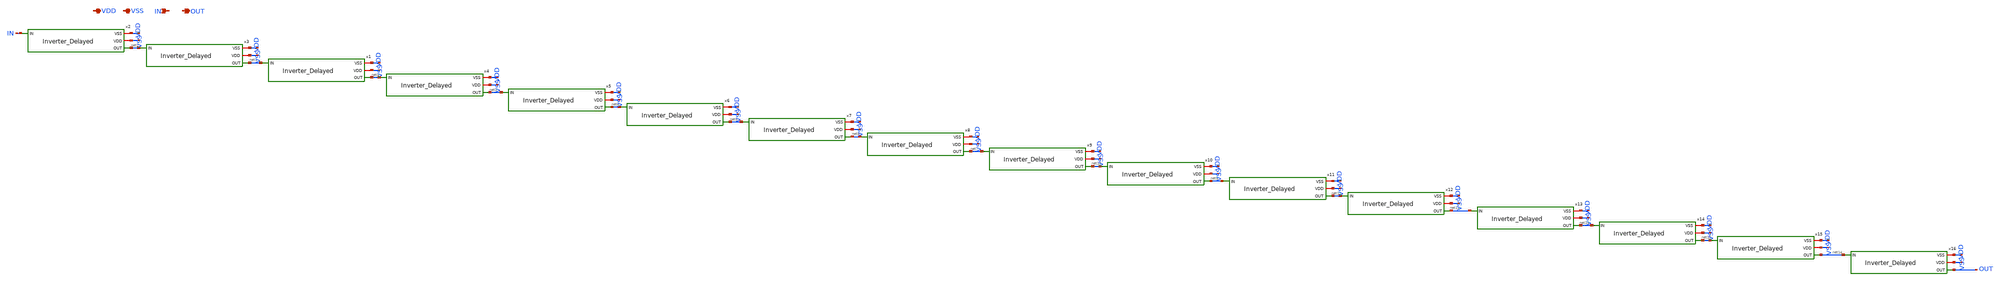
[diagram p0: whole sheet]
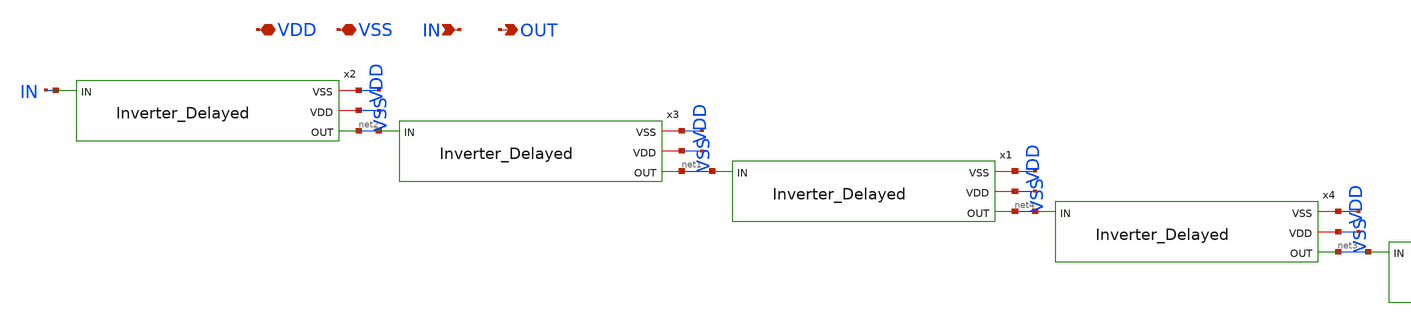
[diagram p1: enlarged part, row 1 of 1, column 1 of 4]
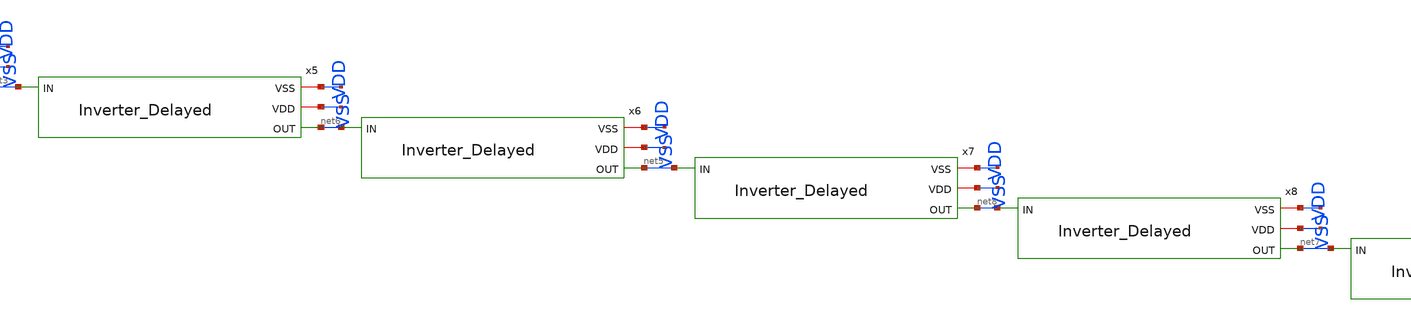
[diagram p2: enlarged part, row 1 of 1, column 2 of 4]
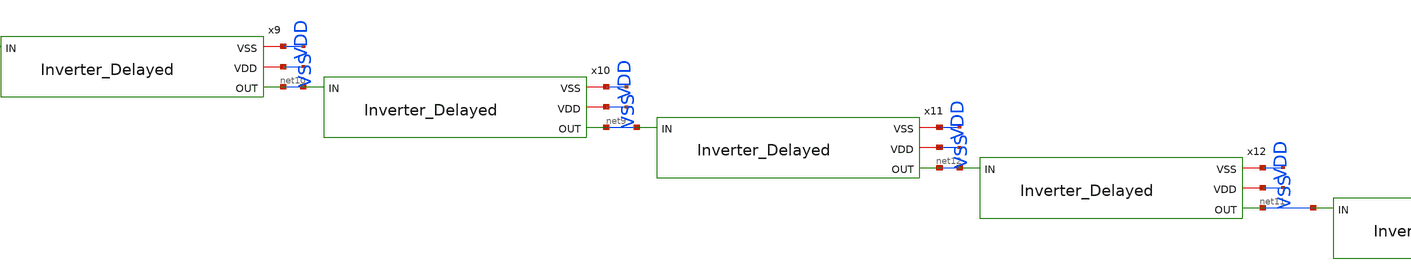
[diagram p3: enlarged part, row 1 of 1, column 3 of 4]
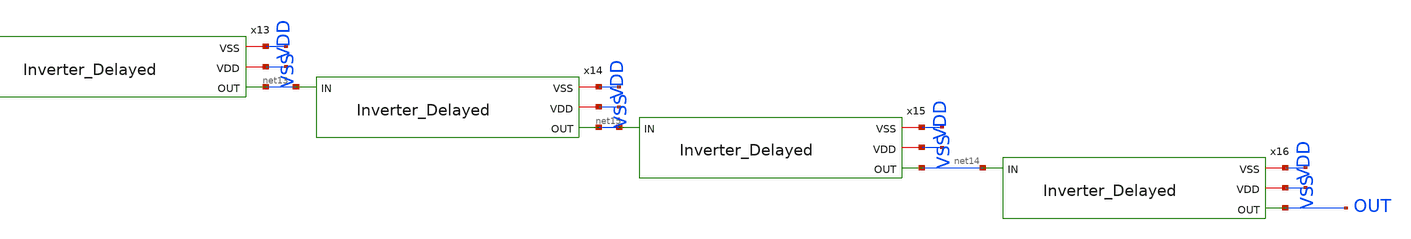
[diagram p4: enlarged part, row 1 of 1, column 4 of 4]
** sch_path: Clock_Generator_PAKISTAN_02/Schematics/Buffer_Delayed1.sch
**.subckt Buffer_Delayed1 VDD VSS IN OUT
*.iopin VDD
*.iopin VSS
*.ipin IN
*.opin OUT
x2 VSS VDD net2 IN Inverter_Delayed
x3 VSS VDD net1 net2 Inverter_Delayed
x1 VSS VDD net4 net1 Inverter_Delayed
x4 VSS VDD net3 net4 Inverter_Delayed
x5 VSS VDD net6 net3 Inverter_Delayed
x6 VSS VDD net5 net6 Inverter_Delayed
x7 VSS VDD net8 net5 Inverter_Delayed
x8 VSS VDD net7 net8 Inverter_Delayed
x9 VSS VDD net10 net7 Inverter_Delayed
x10 VSS VDD net9 net10 Inverter_Delayed
x11 VSS VDD net12 net9 Inverter_Delayed
x12 VSS VDD net11 net12 Inverter_Delayed
x13 VSS VDD net13 net11 Inverter_Delayed
x14 VSS VDD net15 net13 Inverter_Delayed
x15 VSS VDD net14 net15 Inverter_Delayed
x16 VSS VDD OUT net14 Inverter_Delayed
**.ends
.end
